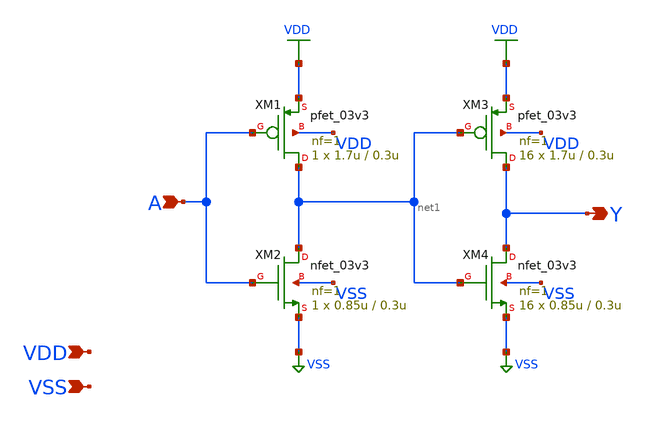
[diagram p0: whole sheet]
** sch_path: gf180mcu_osu_sc_gp12t3v3/xschem/gf180mcu_osu_sc_gp12t3v3__clkbuf_16.sch
**.subckt gf180mcu_osu_sc_gp12t3v3__clkbuf_16 A Y VDD VSS
*.ipin A
*.opin Y
*.ipin VDD
*.ipin VSS
XM1 net1 A VDD VDD pfet_03v3 L=0.3u W=1.7u nf=1 ad='int((nf+1)/2) * W/nf * 0.18u' as='int((nf+2)/2) * W/nf * 0.18u'
+ pd='2*int((nf+1)/2) * (W/nf + 0.18u)' ps='2*int((nf+2)/2) * (W/nf + 0.18u)' nrd='0.18u / W' nrs='0.18u / W'
+ sa=0 sb=0 sd=0 m=1
XM2 net1 A VSS VSS nfet_03v3 L=0.3u W=0.85u nf=1 ad='int((nf+1)/2) * W/nf * 0.18u' as='int((nf+2)/2) * W/nf * 0.18u'
+ pd='2*int((nf+1)/2) * (W/nf + 0.18u)' ps='2*int((nf+2)/2) * (W/nf + 0.18u)' nrd='0.18u / W' nrs='0.18u / W'
+ sa=0 sb=0 sd=0 m=1
XM3 Y net1 VDD VDD pfet_03v3 L=0.3u W=1.7u nf=1 ad='int((nf+1)/2) * W/nf * 0.18u' as='int((nf+2)/2) * W/nf * 0.18u'
+ pd='2*int((nf+1)/2) * (W/nf + 0.18u)' ps='2*int((nf+2)/2) * (W/nf + 0.18u)' nrd='0.18u / W' nrs='0.18u / W'
+ sa=0 sb=0 sd=0 m=16
XM4 Y net1 VSS VSS nfet_03v3 L=0.3u W=0.85u nf=1 ad='int((nf+1)/2) * W/nf * 0.18u' as='int((nf+2)/2) * W/nf * 0.18u'
+ pd='2*int((nf+1)/2) * (W/nf + 0.18u)' ps='2*int((nf+2)/2) * (W/nf + 0.18u)' nrd='0.18u / W' nrs='0.18u / W'
+ sa=0 sb=0 sd=0 m=16
**.ends
.GLOBAL VDD
.GLOBAL VSS
.end
